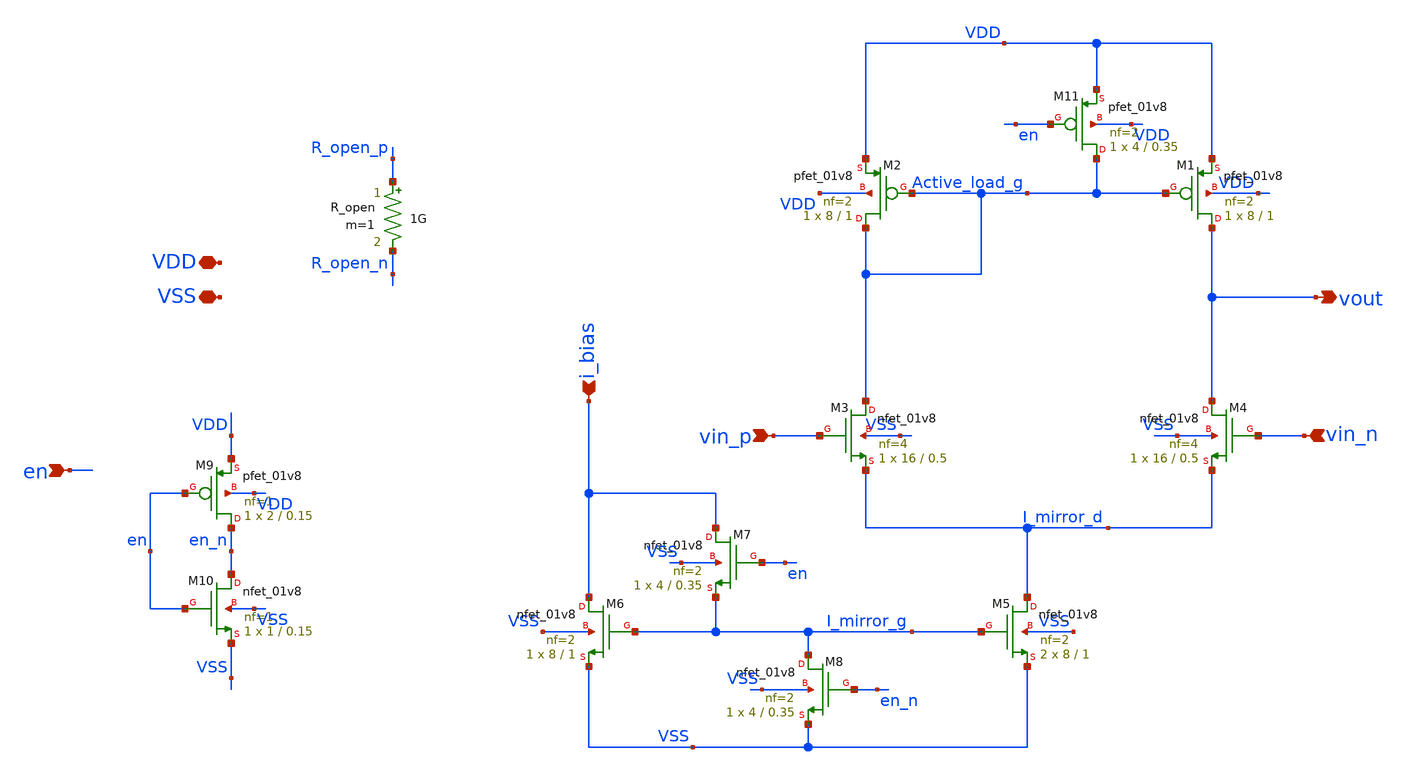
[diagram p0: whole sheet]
** sch_path: ISSCC_2025_V1/xschem/Benchmark_Circuits/OpAmp_Defect/OpAmp.sch
**.subckt OpAmp vin_p vin_n VSS VDD vout i_bias en
*.ipin vin_p
*.ipin vin_n
*.iopin VSS
*.iopin VDD
*.opin vout
*.ipin i_bias
*.ipin en
XM1 vout Active_load_g VDD VDD sky130_fd_pr__pfet_01v8 L=1 W=8 nf=2 ad='int((nf+1)/2) * W/nf * 0.29'
+ as='int((nf+2)/2) * W/nf * 0.29' pd='2*int((nf+1)/2) * (W/nf + 0.29)' ps='2*int((nf+2)/2) * (W/nf + 0.29)'
+ nrd='0.29 / W' nrs='0.29 / W' sa=0 sb=0 sd=0 mult=1 m=1
XM2 Active_load_g Active_load_g VDD VDD sky130_fd_pr__pfet_01v8 L=1 W=8 nf=2 ad='int((nf+1)/2) * W/nf * 0.29'
+ as='int((nf+2)/2) * W/nf * 0.29' pd='2*int((nf+1)/2) * (W/nf + 0.29)' ps='2*int((nf+2)/2) * (W/nf + 0.29)'
+ nrd='0.29 / W' nrs='0.29 / W' sa=0 sb=0 sd=0 mult=1 m=1
XM3 Active_load_g vin_p I_mirror_d VSS sky130_fd_pr__nfet_01v8 L=0.5 W=16 nf=4 ad='int((nf+1)/2) * W/nf * 0.29'
+ as='int((nf+2)/2) * W/nf * 0.29' pd='2*int((nf+1)/2) * (W/nf + 0.29)' ps='2*int((nf+2)/2) * (W/nf + 0.29)'
+ nrd='0.29 / W' nrs='0.29 / W' sa=0 sb=0 sd=0 mult=1 m=1
XM4 vout vin_n I_mirror_d VSS sky130_fd_pr__nfet_01v8 L=0.5 W=16 nf=4 ad='int((nf+1)/2) * W/nf * 0.29'
+ as='int((nf+2)/2) * W/nf * 0.29' pd='2*int((nf+1)/2) * (W/nf + 0.29)' ps='2*int((nf+2)/2) * (W/nf + 0.29)'
+ nrd='0.29 / W' nrs='0.29 / W' sa=0 sb=0 sd=0 mult=1 m=1
XM5 I_mirror_d I_mirror_g VSS VSS sky130_fd_pr__nfet_01v8 L=1 W=8 nf=2 ad='int((nf+1)/2) * W/nf * 0.29'
+ as='int((nf+2)/2) * W/nf * 0.29' pd='2*int((nf+1)/2) * (W/nf + 0.29)' ps='2*int((nf+2)/2) * (W/nf + 0.29)'
+ nrd='0.29 / W' nrs='0.29 / W' sa=0 sb=0 sd=0 mult=2 m=2
XM6 i_bias I_mirror_g VSS VSS sky130_fd_pr__nfet_01v8 L=1 W=8 nf=2 ad='int((nf+1)/2) * W/nf * 0.29' as='int((nf+2)/2) * W/nf * 0.29'
+ pd='2*int((nf+1)/2) * (W/nf + 0.29)' ps='2*int((nf+2)/2) * (W/nf + 0.29)' nrd='0.29 / W' nrs='0.29 / W'
+ sa=0 sb=0 sd=0 mult=1 m=1
XM9 en_n en VDD VDD sky130_fd_pr__pfet_01v8 L=0.15 W=2 nf=1 ad='int((nf+1)/2) * W/nf * 0.29' as='int((nf+2)/2) * W/nf * 0.29'
+ pd='2*int((nf+1)/2) * (W/nf + 0.29)' ps='2*int((nf+2)/2) * (W/nf + 0.29)' nrd='0.29 / W' nrs='0.29 / W'
+ sa=0 sb=0 sd=0 mult=1 m=1
XM10 en_n en VSS VSS sky130_fd_pr__nfet_01v8 L=0.15 W=1 nf=1 ad='int((nf+1)/2) * W/nf * 0.29' as='int((nf+2)/2) * W/nf * 0.29'
+ pd='2*int((nf+1)/2) * (W/nf + 0.29)' ps='2*int((nf+2)/2) * (W/nf + 0.29)' nrd='0.29 / W' nrs='0.29 / W'
+ sa=0 sb=0 sd=0 mult=1 m=1
XM7 i_bias en I_mirror_g VSS sky130_fd_pr__nfet_01v8 L=0.35 W=4 nf=2 ad='int((nf+1)/2) * W/nf * 0.29'
+ as='int((nf+2)/2) * W/nf * 0.29' pd='2*int((nf+1)/2) * (W/nf + 0.29)' ps='2*int((nf+2)/2) * (W/nf + 0.29)'
+ nrd='0.29 / W' nrs='0.29 / W' sa=0 sb=0 sd=0 mult=1 m=1
XM8 I_mirror_g en_n VSS VSS sky130_fd_pr__nfet_01v8 L=0.35 W=4 nf=2 ad='int((nf+1)/2) * W/nf * 0.29'
+ as='int((nf+2)/2) * W/nf * 0.29' pd='2*int((nf+1)/2) * (W/nf + 0.29)' ps='2*int((nf+2)/2) * (W/nf + 0.29)'
+ nrd='0.29 / W' nrs='0.29 / W' sa=0 sb=0 sd=0 mult=1 m=1
XM11 Active_load_g en VDD VDD sky130_fd_pr__pfet_01v8 L=0.35 W=4 nf=2 ad='int((nf+1)/2) * W/nf * 0.29'
+ as='int((nf+2)/2) * W/nf * 0.29' pd='2*int((nf+1)/2) * (W/nf + 0.29)' ps='2*int((nf+2)/2) * (W/nf + 0.29)'
+ nrd='0.29 / W' nrs='0.29 / W' sa=0 sb=0 sd=0 mult=1 m=1
R_open R_open_p R_open_n 1G m=1
**.ends
.end
